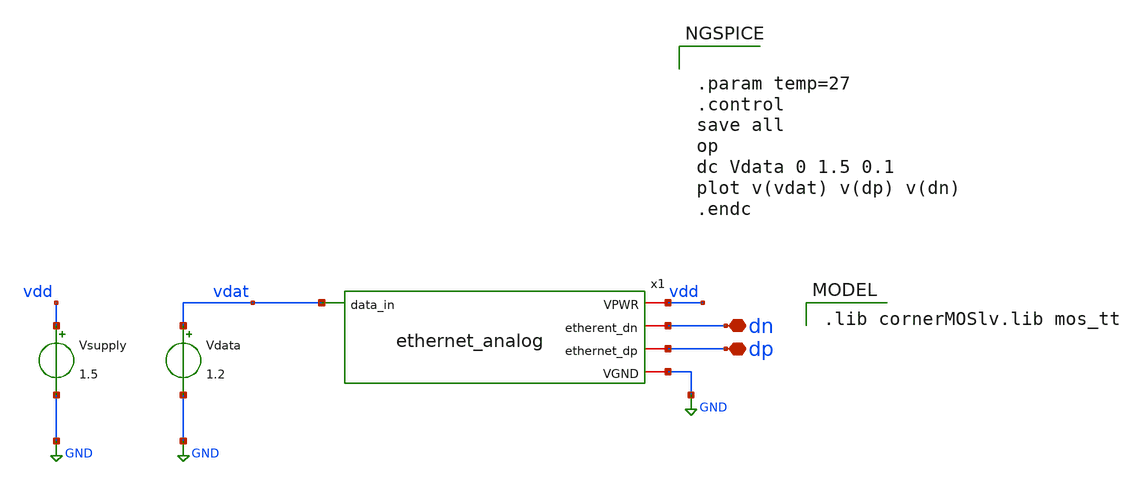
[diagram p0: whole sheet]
** sch_path: xschem/ethernet_analog_tb.sch
**.subckt ethernet_analog_tb dn dp
*.iopin dn
*.iopin dp
Vdata vdat GND 1.2
Vsupply vdd GND 1.5
x1 vdd vdat dn dp GND ethernet_analog
**** begin user architecture code


.param temp=27
.control
save all
op
dc Vdata 0 1.5 0.1
plot v(vdat) v(dp) v(dn)
.endc


 .lib cornerMOSlv.lib mos_tt

**** end user architecture code
**.ends

* expanding   symbol:  /home/pc/heichips25-ethernet/xschem/ethernet_analog.sym # of pins=5
** sym_path: xschem/ethernet_analog.sym
** sch_path: xschem/ethernet_analog.sch
.subckt ethernet_analog VPWR data_in etherent_dn ethernet_dp VGND
*.ipin data_in
*.iopin etherent_dn
*.iopin VGND
*.iopin VPWR
*.iopin ethernet_dp
XM2 etherent_dn data_in VGND VGND sg13_lv_nmos w=0.15u l=0.13u ng=1 m=1 mm_ok=1
XM1 etherent_dn data_in VPWR VPWR sg13_lv_pmos w=0.15u l=0.13u ng=1 m=1 mm_ok=1
R1 ethernet_dp data_in 1n m=1
.ends

.GLOBAL GND
.end
